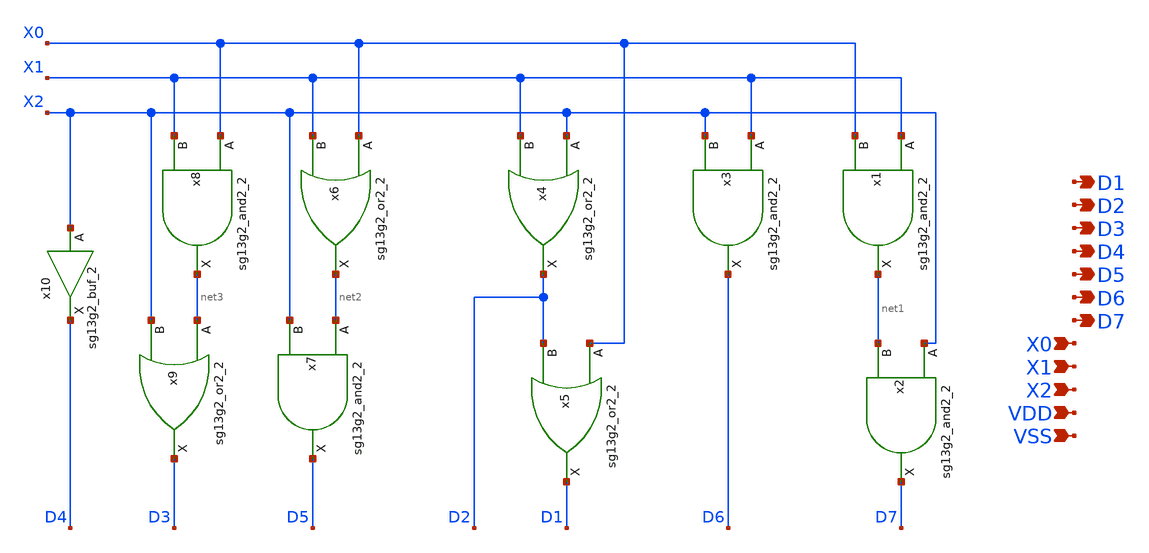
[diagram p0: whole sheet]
** sch_path: klayout/xschem/thermo_decoder.sch
* IHP-GmbH/IHP-Open-PDK/ihp-sg13g2/libs.tech/xschem/sg13g2_stdcells/sg13g2_or2_2.sch:
* Copyright 2023 IHP PDK Authors
* Licensed under the Apache License, Version 2.0 (the "License");
**.subckt thermo_decoder X2 X1 X0 D7 D6 D5 D4 D3 D1 D2 VDD VSS
*.ipin X2
*.ipin X1
*.ipin X0
*.opin D7
*.opin D6
*.opin D5
*.opin D4
*.opin D3
*.opin D1
*.opin D2
*.ipin VDD
*.ipin VSS
x1 net1 X1 X0 VDD VSS sg13g2_and2_2
x2 D7 X2 net1 VDD VSS sg13g2_and2_2
x3 D6 X1 X2 VDD VSS sg13g2_and2_2
x4 D2 X2 X1 VDD VSS sg13g2_or2_2
x5 D1 X0 D2 VDD VSS sg13g2_or2_2
x6 net2 X0 X1 VDD VSS sg13g2_or2_2
x7 D5 net2 X2 VDD VSS sg13g2_and2_2
x8 net3 X0 X1 VDD VSS sg13g2_and2_2
x9 D3 net3 X2 VDD VSS sg13g2_or2_2
x10 D4 X2 VDD VSS sg13g2_buf_2
**.ends

* expanding   symbol:  sg13g2_stdcells/sg13g2_and2_2.sym # of pins=3
** sym_path: sg13g2_stdcells/sg13g2_and2_2.sym
** sch_path: sg13g2_stdcells/sg13g2_and2_2.sch
.subckt sg13g2_and2_2 X A B VDD VSS
*.ipin A
*.ipin B
*.opin X
*.iopin VDD
*.iopin VSS
XM1 net1 A net2 VSS sg13_lv_nmos w=640.00n l=130.00n ng=1 m=1 mm_ok=1
XM2 net2 B VSS VSS sg13_lv_nmos w=640.00n l=130.00n ng=1 m=1 mm_ok=1
XM3 X net1 VSS VSS sg13_lv_nmos w=1.48u l=130.00n ng=2 m=1 mm_ok=1
XM4 net1 B VDD VDD sg13_lv_pmos w=840.00n l=130.00n ng=1 m=1 mm_ok=1
XM5 net1 A VDD VDD sg13_lv_pmos w=840.00n l=130.00n ng=1 m=1 mm_ok=1
XM6 X net1 VDD VDD sg13_lv_pmos w=2.24u l=130.00n ng=2 m=1 mm_ok=1
.ends


* expanding   symbol:  sg13g2_stdcells/sg13g2_or2_2.sym # of pins=3
** sym_path: sg13g2_stdcells/sg13g2_or2_2.sym
** sch_path: sg13g2_stdcells/sg13g2_or2_2.sch
.subckt sg13g2_or2_2 X A B VDD VSS
*.opin X
*.ipin B
*.ipin A
*.iopin VDD
*.iopin VSS
XM1 net1 B VSS VSS sg13_lv_nmos w=550.00n l=130.00n ng=1 m=1 mm_ok=1
XM2 net1 A VSS VSS sg13_lv_nmos w=550.00n l=130.00n ng=1 m=1 mm_ok=1
XM3 X net1 VSS VSS sg13_lv_nmos w=1.48u l=130.00n ng=2 m=1 mm_ok=1
XM4 net2 A VDD VDD sg13_lv_pmos w=840.00n l=130.00n ng=1 m=1 mm_ok=1
XM5 net1 B net2 VDD sg13_lv_pmos w=840.00n l=130.00n ng=1 m=1 mm_ok=1
XM6 X net1 VDD VDD sg13_lv_pmos w=2.24u l=130.00n ng=2 m=1 mm_ok=1
.ends


* expanding   symbol:  sg13g2_stdcells/sg13g2_buf_2.sym # of pins=2
** sym_path: sg13g2_stdcells/sg13g2_buf_2.sym
** sch_path: sg13g2_stdcells/sg13g2_buf_2.sch
.subckt sg13g2_buf_2 X A VDD VSS
*.ipin A
*.opin X
*.iopin VDD
*.iopin VSS
XM1 net1 A VSS VSS sg13_lv_nmos w=640.00n l=130.00n ng=1 m=1 mm_ok=1
XM2 X net1 VSS VSS sg13_lv_nmos w=1.48u l=130.00n ng=2 m=1 mm_ok=1
XM3 net1 A VDD VDD sg13_lv_pmos w=1.000u l=130.00n ng=1 m=1 mm_ok=1
XM4 X net1 VDD VDD sg13_lv_pmos w=2.24u l=130.00n ng=2 m=1 mm_ok=1
.ends

.end
